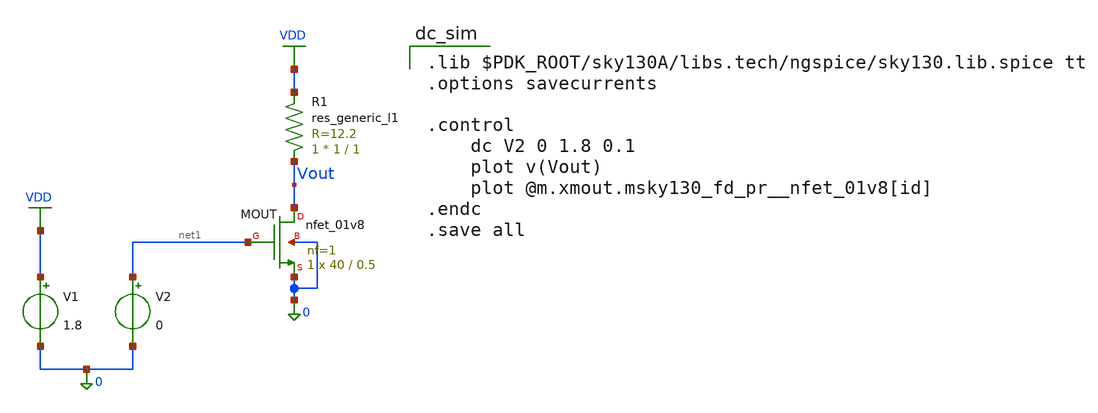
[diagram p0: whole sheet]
** sch_path: designs_backup/designs/test_cir.sch
**.subckt test_cir
XMOUT Vout net1 0 0 sky130_fd_pr__nfet_01v8 L=0.5 W=40 nf=1 ad='int((1 + 1)/2) * 40 / 1 * 0.29' as='int((1 + 2)/2) * 40 / 1 * 0.29'
+ pd='2*int((1 + 1)/2) * (40 / 1 + 0.29)' ps='2*int((1 + 2)/2) * (40 / 1 + 0.29)' nrd='0.29 / 40 ' nrs='0.29 / 40 '
+ sa=0 sb=0 sd=0 mult=1 m=1
R1 Vout VDD sky130_fd_pr__res_generic_l1 W=1 L=1 m=1
V1 VDD 0 1.8
V2 net1 0 0
**** begin user architecture code

.lib $PDK_ROOT/sky130A/libs.tech/ngspice/sky130.lib.spice tt
.options savecurrents

.control
	dc V2 0 1.8 0.1
	plot v(Vout)
	plot @m.xmout.msky130_fd_pr__nfet_01v8[id]
.endc
.save all

**** end user architecture code
**.ends
.GLOBAL VDD
.end
